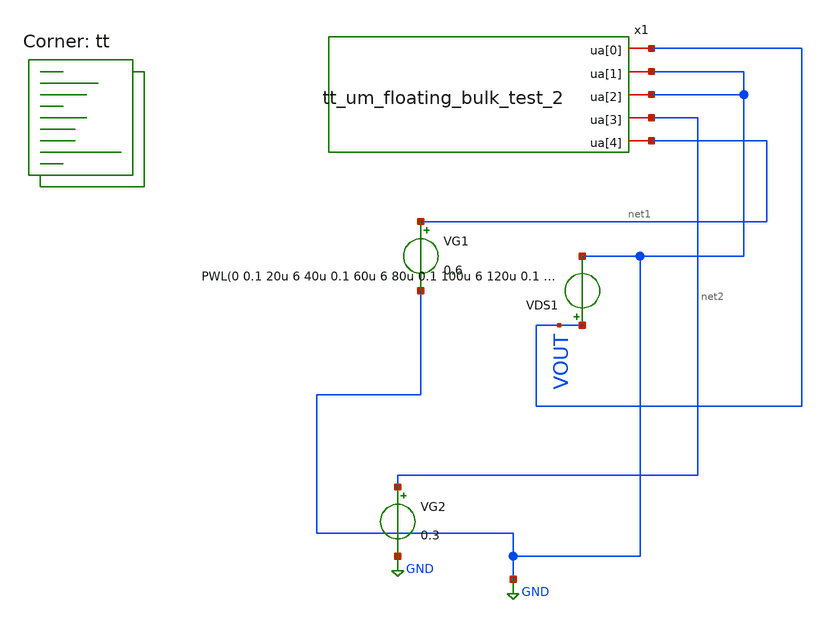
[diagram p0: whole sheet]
** sch_path: xschem/tt_um_floating_bulk_test_2_TB.sch

.include /home/rogel/pdk/sky130A/libs.ref/sky130_fd_sc_hd/spice/sky130_fd_sc_hd.spice

**.subckt tt_um_floating_bulk_test_2_TB
VG2 net2 GND 0.3
VG1 net1 GND 0.6
VDS1 VOUT GND PWL(0 0.1 20u 6 40u 0.1 60u 6 80u 0.1 100u 6 120u 0.1 140u 6 160u 0.1 180u 6 200u 0.1
+ 220u 6 240u 0.1)
x1 GND GND net2 VOUT net1 tt_um_floating_bulk_test_2
**** begin user architecture code
.lib $::SKYWATER_MODELS/sky130.lib.spice tt


.control
set num_threads=8
option klu
save i(VDS1) v(VOUT)
foreach val_vg1 1.0 1.2 1.4
    alter VG1 $val_vg1
    foreach val_vg2 0.5 0.6 0.7
        alter VG2 $val_vg2

        tran 1u 240u
        let idrain = -i(VDS1)
    end
end
*plot tran1.idrain vs tran1.v(VOUT) tran2.idrain vs tran2.v(VOUT) tran3.idrain vs tran3.v(VOUT) tran4.idrain
*+ vs tran4.v(VOUT) tran5.idrain vs tran5.v(VOUT) tran6.idrain vs tran6.v(VOUT) tran7.idrain vs tran7.v(VOUT)
*+ tran8.idrain vs tran8.v(VOUT) tran9.idrain vs tran9.v(VOUT) ylog title 'Optimizacion: Buscando la maxima ventana de histeresis'
plot tran2.idrain vs tran2.v(VOUT) title 'VG1 = 1V, VG2 = 0.7V'
write tt_um_floating_bulk_test_2_TB.raw
.endc


**** end user architecture code
**.ends

* expanding   symbol:  /home/rogel/xschem_attempts/VALTIERRA_PROJECT/tt_um_floating_bulk_test_2.sym
*+ # of pins=5
** sym_path: xschem/tt_um_floating_bulk_test_2.sym
** sch_path: xschem/tt_um_floating_bulk_test_2.sch
.subckt tt_um_floating_bulk_test_2 ua[1] ua[2] ua[3] ua[0] ua[4]
*.iopin ua[0]
*.iopin ua[1]
*.iopin ua[2]
*.iopin ua[3]
*.iopin ua[4]
**** begin user architecture code


* SPICE3 file created from tt_um_floating_bulk_test_2.ext - technology: sky130A

X0 ua[0] ua[4] ua[1] w_22268_1880# sky130_fd_pr__nfet_01v8 ad=0.1218 pd=1.42 as=0.1218 ps=1.42
+ w=0.42 l=0.15
X1 ua[2] ua[3] w_22268_1880# ua[2] sky130_fd_pr__nfet_01v8 ad=0.1218 pd=1.42 as=0.1218 ps=1.42
+ w=0.42 l=0.15
C0 uio_out[2] uio_out[3] 0.03102f
C1 ua[0] ua[3] 0.01547f
C2 ui_in[2] ui_in[3] 0.03102f
C3 ua[1] w_22268_1880# 0.47259f
C4 uio_in[5] uio_in[4] 0.03102f
C5 uio_oe[7] uio_oe[6] 0.03102f
C6 ua[4] ua[0] 0.54542f
C7 w_22268_1880# ua[3] 0.07418f
C8 uio_oe[5] uio_oe[6] 0.03102f
C9 uio_out[7] uio_oe[0] 0.03102f
C10 uio_oe[0] uio_oe[1] 0.03102f
C11 ua[4] w_22268_1880# 0.275f
C12 uio_out[6] uio_out[5] 0.03102f
C13 uio_in[3] uio_in[2] 0.03102f
C14 uio_oe[2] uio_oe[1] 0.03102f
C15 uio_in[2] uio_in[1] 0.03102f
C16 uo_out[2] uo_out[1] 0.03102f
C17 ui_in[6] ui_in[5] 0.03102f
C18 ui_in[4] ui_in[3] 0.03102f
C19 uio_in[7] uo_out[0] 0.03102f
C20 ua[4] ua[1] 0.04778f
C21 uo_out[3] uo_out[4] 0.03102f
C22 uo_out[7] uio_out[0] 0.03102f
C23 ui_in[0] rst_n 0.03102f
C24 uio_in[3] uio_in[4] 0.03102f
C25 clk rst_n 0.03102f
C26 VDPWR VGND 12.9181f
C27 uio_out[2] uio_out[1] 0.03102f
C28 uio_in[0] uio_in[1] 0.03102f
C29 ui_in[6] ui_in[7] 0.03102f
C30 ena clk 0.03102f
C31 uio_out[4] uio_out[3] 0.03102f
C32 uio_oe[2] uio_oe[3] 0.03102f
C33 uo_out[3] uo_out[2] 0.03102f
C34 uio_in[5] uio_in[6] 0.03102f
C35 w_22268_1880# ua[0] 3.17898f
C36 uio_in[7] uio_in[6] 0.03102f
C37 uio_out[7] uio_out[6] 0.03102f
C38 ui_in[4] ui_in[5] 0.03102f
C39 uo_out[4] uo_out[5] 0.03102f
C40 uo_out[6] uo_out[5] 0.03102f
C41 uio_oe[4] uio_oe[3] 0.03102f
C42 ui_in[2] ui_in[1] 0.03102f
C43 uio_out[1] uio_out[0] 0.03102f
C44 uo_out[7] uo_out[6] 0.03102f
C45 ui_in[0] ui_in[1] 0.03102f
C46 uio_in[0] ui_in[7] 0.03102f
C47 uio_oe[4] uio_oe[5] 0.03102f
C48 uio_out[4] uio_out[5] 0.03102f
C49 uo_out[1] uo_out[0] 0.03102f
C50 ua[1] ua[0] 0.40322f
C51 ua[5] ua[2] 0.14696f
C52 ua[6] ua[2] 0.14696f
C53 ua[7] ua[2] 0.14696f
C54 VGND ua[2] 12.5347f
C55 VDPWR ua[2] 12.5347f
C56 ena ua[2] 0.07038f
C57 clk ua[2] 0.04288f
C58 rst_n ua[2] 0.04288f
C59 ui_in[0] ua[2] 0.04288f
C60 ui_in[1] ua[2] 0.04288f
C61 ui_in[2] ua[2] 0.04288f
C62 ui_in[3] ua[2] 0.04288f
C63 ui_in[4] ua[2] 0.04288f
C64 ui_in[5] ua[2] 0.04288f
C65 ui_in[6] ua[2] 0.04288f
C66 ui_in[7] ua[2] 0.04288f
C67 uio_in[0] ua[2] 0.04288f
C68 uio_in[1] ua[2] 0.04288f
C69 uio_in[2] ua[2] 0.04288f
C70 uio_in[3] ua[2] 0.04288f
C71 uio_in[4] ua[2] 0.04288f
C72 uio_in[5] ua[2] 0.04288f
C73 uio_in[6] ua[2] 0.04288f
C74 uio_in[7] ua[2] 0.04288f
C75 uo_out[0] ua[2] 0.04288f
C76 uo_out[1] ua[2] 0.04288f
C77 uo_out[2] ua[2] 0.04288f
C78 uo_out[3] ua[2] 0.04288f
C79 uo_out[4] ua[2] 0.04288f
C80 uo_out[5] ua[2] 0.04288f
C81 uo_out[6] ua[2] 0.04288f
C82 uo_out[7] ua[2] 0.04288f
C83 uio_out[0] ua[2] 0.04288f
C84 uio_out[1] ua[2] 0.04288f
C85 uio_out[2] ua[2] 0.04288f
C86 uio_out[3] ua[2] 0.04288f
C87 uio_out[4] ua[2] 0.04288f
C88 uio_out[5] ua[2] 0.04288f
C89 uio_out[6] ua[2] 0.04288f
C90 uio_out[7] ua[2] 0.04288f
C91 uio_oe[0] ua[2] 0.04288f
C92 uio_oe[1] ua[2] 0.04288f
C93 uio_oe[2] ua[2] 0.04288f
C94 uio_oe[3] ua[2] 0.04288f
C95 uio_oe[4] ua[2] 0.04288f
C96 uio_oe[5] ua[2] 0.04288f
C97 uio_oe[6] ua[2] 0.04288f
C98 uio_oe[7] ua[2] 0.07038f
C99 ua[3] ua[2] 2.55804f
C100 ua[1] ua[2] 1.49665f
C101 ua[4] ua[2] 5.50486f
C102 w_22268_1880# ua[2] 0.53587f ;**FLOATING
C103 ua[0] ua[2] 13.77466f


**** end user architecture code
.ends

.GLOBAL GND
.end
